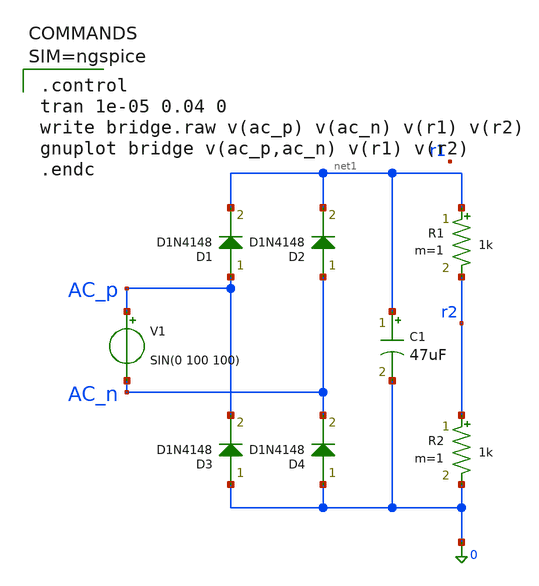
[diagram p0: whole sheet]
** sch_path: tests/bridge/bridge_annotation.sch
**.subckt bridge_annotation
R1 net1 r2 1k m=1
R2 r2 0 1k m=1
D1 AC_p net1 D1N4148 area=1
D2 AC_n net1 D1N4148 area=1
D3 0 AC_p D1N4148 area=1
D4 0 AC_n D1N4148 area=1
C1 net1 0 47uF m=1
V1 AC_p AC_n SIN(0 100 100)
**** begin user architecture code


.control
tran 1e-05 0.04 0
write bridge.raw v(ac_p) v(ac_n) v(r1) v(r2)
gnuplot bridge v(ac_p,ac_n) v(r1) v(r2)
.endc



**** end user architecture code
**.ends
**** begin user architecture code

.model D1N4148 D(Is=2.55e-9 N=1.75 Rs=42e-3 Cj0=42.4e-12 Vj=0.75 M=0.333 Fc=0.5 Tt=4.32e-6 Bv=800
+ Ibv=80e-6 Af=1 Kf=0)

**** end user architecture code
.end
